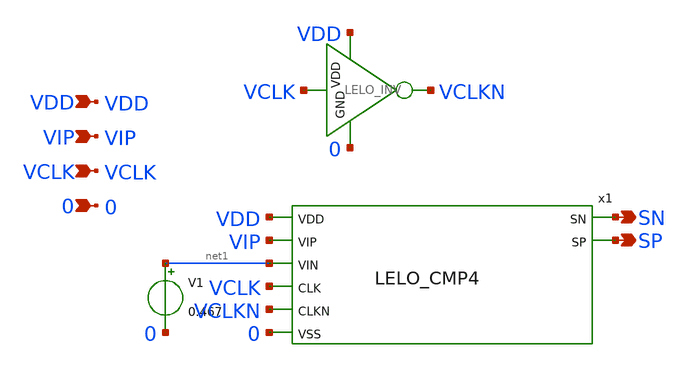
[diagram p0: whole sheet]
** sch_path: design/LELO_SVOD_SKY130A/LELO_SVOD_CMP_TB.sch
**.subckt LELO_SVOD_CMP_TB VDD SN 0 SP VCLK VIP
*.ipin VDD
*.opin SN
*.ipin 0
*.opin SP
*.ipin VCLK
*.ipin VIP
x2 VDD VCLK VCLKN 0 LELO_INV
V1 net1 0 0.467
x1 SN SP VDD VIP net1 VCLK VCLKN 0 LELO_CMP4
**.ends
.end
